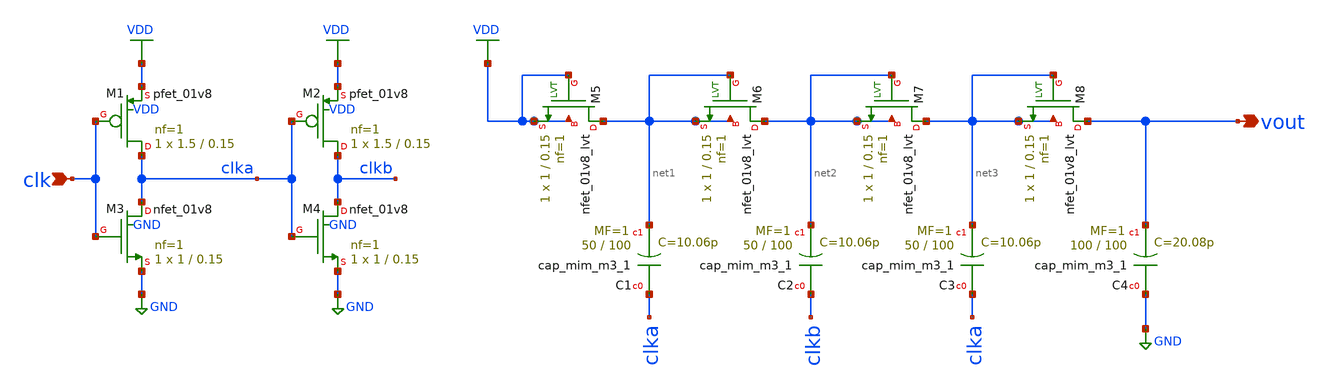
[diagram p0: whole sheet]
** sch_path: xschem/dickson.sch
**.subckt dickson clk vout
*.ipin clk
*.opin vout
XM1 clka clk VDD VDD sky130_fd_pr__pfet_01v8 L=0.15 W=1.5 nf=1 ad='int((nf+1)/2) * W/nf * 0.29' as='int((nf+2)/2) * W/nf * 0.29'
+ pd='2*int((nf+1)/2) * (W/nf + 0.29)' ps='2*int((nf+2)/2) * (W/nf + 0.29)' nrd='0.29 / W' nrs='0.29 / W'
+ sa=0 sb=0 sd=0 mult=1 m=1
XM3 clka clk GND GND sky130_fd_pr__nfet_01v8 L=0.15 W=1 nf=1 ad='int((nf+1)/2) * W/nf * 0.29' as='int((nf+2)/2) * W/nf * 0.29'
+ pd='2*int((nf+1)/2) * (W/nf + 0.29)' ps='2*int((nf+2)/2) * (W/nf + 0.29)' nrd='0.29 / W' nrs='0.29 / W'
+ sa=0 sb=0 sd=0 mult=1 m=1
XM2 clkb clka VDD VDD sky130_fd_pr__pfet_01v8 L=0.15 W=1.5 nf=1 ad='int((nf+1)/2) * W/nf * 0.29' as='int((nf+2)/2) * W/nf * 0.29'
+ pd='2*int((nf+1)/2) * (W/nf + 0.29)' ps='2*int((nf+2)/2) * (W/nf + 0.29)' nrd='0.29 / W' nrs='0.29 / W'
+ sa=0 sb=0 sd=0 mult=1 m=1
XM4 clkb clka GND GND sky130_fd_pr__nfet_01v8 L=0.15 W=1 nf=1 ad='int((nf+1)/2) * W/nf * 0.29' as='int((nf+2)/2) * W/nf * 0.29'
+ pd='2*int((nf+1)/2) * (W/nf + 0.29)' ps='2*int((nf+2)/2) * (W/nf + 0.29)' nrd='0.29 / W' nrs='0.29 / W'
+ sa=0 sb=0 sd=0 mult=1 m=1
XC3 clka net3 sky130_fd_pr__cap_mim_m3_1 W=50 L=100 MF=1 m=1
XM5 net1 VDD VDD VDD sky130_fd_pr__nfet_01v8_lvt L=0.15 W=1 nf=1 ad='int((nf+1)/2) * W/nf * 0.29' as='int((nf+2)/2) * W/nf * 0.29'
+ pd='2*int((nf+1)/2) * (W/nf + 0.29)' ps='2*int((nf+2)/2) * (W/nf + 0.29)' nrd='0.29 / W' nrs='0.29 / W'
+ sa=0 sb=0 sd=0 mult=1 m=1
XC1 clka net1 sky130_fd_pr__cap_mim_m3_1 W=50 L=100 MF=1 m=1
XM6 net2 net1 net1 net1 sky130_fd_pr__nfet_01v8_lvt L=0.15 W=1 nf=1 ad='int((nf+1)/2) * W/nf * 0.29'
+ as='int((nf+2)/2) * W/nf * 0.29' pd='2*int((nf+1)/2) * (W/nf + 0.29)' ps='2*int((nf+2)/2) * (W/nf + 0.29)'
+ nrd='0.29 / W' nrs='0.29 / W' sa=0 sb=0 sd=0 mult=1 m=1
XM7 net3 net2 net2 net2 sky130_fd_pr__nfet_01v8_lvt L=0.15 W=1 nf=1 ad='int((nf+1)/2) * W/nf * 0.29'
+ as='int((nf+2)/2) * W/nf * 0.29' pd='2*int((nf+1)/2) * (W/nf + 0.29)' ps='2*int((nf+2)/2) * (W/nf + 0.29)'
+ nrd='0.29 / W' nrs='0.29 / W' sa=0 sb=0 sd=0 mult=1 m=1
XC2 clkb net2 sky130_fd_pr__cap_mim_m3_1 W=50 L=100 MF=1 m=1
XM8 vout net3 net3 net3 sky130_fd_pr__nfet_01v8_lvt L=0.15 W=1 nf=1 ad='int((nf+1)/2) * W/nf * 0.29'
+ as='int((nf+2)/2) * W/nf * 0.29' pd='2*int((nf+1)/2) * (W/nf + 0.29)' ps='2*int((nf+2)/2) * (W/nf + 0.29)'
+ nrd='0.29 / W' nrs='0.29 / W' sa=0 sb=0 sd=0 mult=1 m=1
XC4 GND vout sky130_fd_pr__cap_mim_m3_1 W=100 L=100 MF=1 m=1
**.ends
.GLOBAL GND
.GLOBAL VDD
.end
